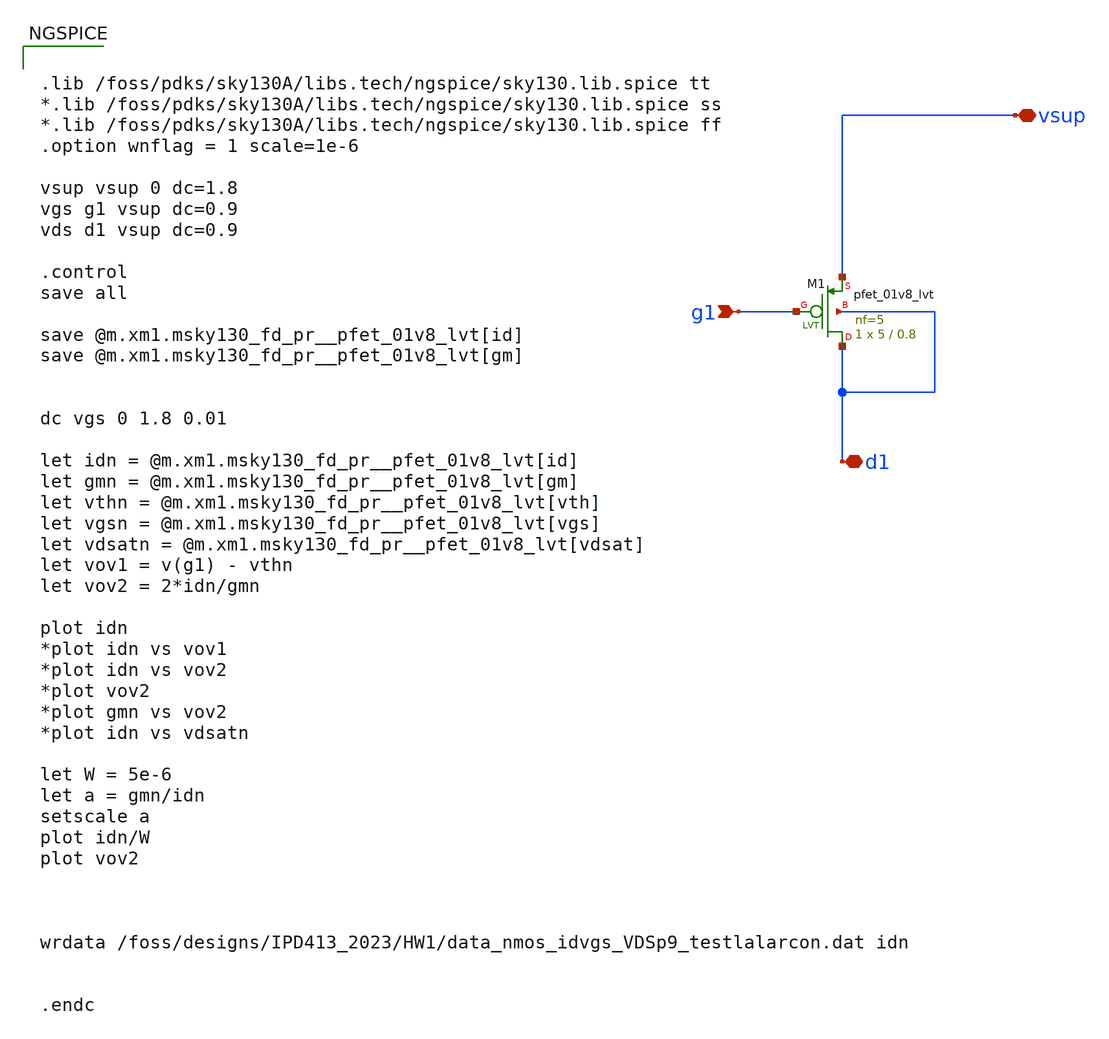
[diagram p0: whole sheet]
** sch_path: pmos_charac_IPD413HW2_LVT_M3n4.sch
**.subckt pmos_charac_IPD413HW2_LVT_M3n4 g1 d1 vsup
*.ipin g1
*.iopin d1
*.iopin vsup
XM1 d1 g1 vsup d1 sky130_fd_pr__pfet_01v8_lvt L=0.8 W=5 nf=5 ad='int((nf+1)/2) * W/nf * 0.29' as='int((nf+2)/2) * W/nf * 0.29'
+ pd='2*int((nf+1)/2) * (W/nf + 0.29)' ps='2*int((nf+2)/2) * (W/nf + 0.29)' nrd='0.29 / W' nrs='0.29 / W'
+ sa=0 sb=0 sd=0 mult=1 m=1
**** begin user architecture code


.lib /foss/pdks/sky130A/libs.tech/ngspice/sky130.lib.spice tt
*.lib /foss/pdks/sky130A/libs.tech/ngspice/sky130.lib.spice ss
*.lib /foss/pdks/sky130A/libs.tech/ngspice/sky130.lib.spice ff
.option wnflag = 1 scale=1e-6

vsup vsup 0 dc=1.8
vgs g1 vsup dc=0.9
vds d1 vsup dc=0.9

.control
save all

save @m.xm1.msky130_fd_pr__pfet_01v8_lvt[id]
save @m.xm1.msky130_fd_pr__pfet_01v8_lvt[gm]


dc vgs 0 1.8 0.01

let idn = @m.xm1.msky130_fd_pr__pfet_01v8_lvt[id]
let gmn = @m.xm1.msky130_fd_pr__pfet_01v8_lvt[gm]
let vthn = @m.xm1.msky130_fd_pr__pfet_01v8_lvt[vth]
let vgsn = @m.xm1.msky130_fd_pr__pfet_01v8_lvt[vgs]
let vdsatn = @m.xm1.msky130_fd_pr__pfet_01v8_lvt[vdsat]
let vov1 = v(g1) - vthn
let vov2 = 2*idn/gmn

plot idn
*plot idn vs vov1
*plot idn vs vov2
*plot vov2
*plot gmn vs vov2
*plot idn vs vdsatn

let W = 5e-6
let a = gmn/idn
setscale a
plot idn/W
plot vov2



wrdata /foss/designs/IPD413_2023/HW1/data_nmos_idvgs_VDSp9_testlalarcon.dat idn


.endc


**** end user architecture code
**.ends
.end
